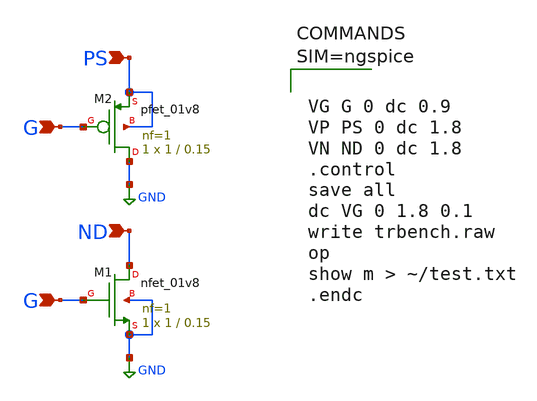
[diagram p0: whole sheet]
** sch_path: trbench.sch
**.subckt trbench ND G G PS
*.ipin ND
*.ipin G
*.ipin G
*.ipin PS
XM1 ND G GND GND sky130_fd_pr__nfet_01v8 L=0.15 W=1 nf=1 ad='int((nf+1)/2) * W/nf * 0.29' as='int((nf+2)/2) * W/nf * 0.29'
+ pd='2*int((nf+1)/2) * (W/nf + 0.29)' ps='2*int((nf+2)/2) * (W/nf + 0.29)' nrd='0.29 / W' nrs='0.29 / W'
+ sa=0 sb=0 sd=0 mult=1 m=1
XM2 GND G PS PS sky130_fd_pr__pfet_01v8 L=0.15 W=1 nf=1 ad='int((nf+1)/2) * W/nf * 0.29' as='int((nf+2)/2) * W/nf * 0.29'
+ pd='2*int((nf+1)/2) * (W/nf + 0.29)' ps='2*int((nf+2)/2) * (W/nf + 0.29)' nrd='0.29 / W' nrs='0.29 / W'
+ sa=0 sb=0 sd=0 mult=1 m=1
**** begin user architecture code



VG G 0 dc 0.9
VP PS 0 dc 1.8
VN ND 0 dc 1.8
.control
save all
dc VG 0 1.8 0.1
write trbench.raw
op
show m > ~/test.txt
.endc



 .param mc_mm_switch=0
.param mc_pr_switch=0
.include $::SKYWATER_MODELS/corners/tt.spice
.include $::SKYWATER_MODELS/r+c/res_typical__cap_typical.spice
.include $::SKYWATER_MODELS/r+c/res_typical__cap_typical__lin.spice
.include $::SKYWATER_MODELS/corners/tt/specialized_cells.spice
.include $::SKYWATER_STDCELLS/sky130_fd_sc_hd.spice

**** end user architecture code
**.ends
.GLOBAL GND
.end
